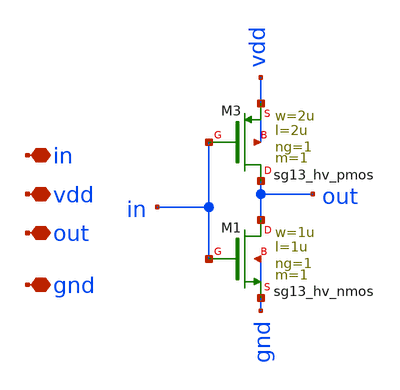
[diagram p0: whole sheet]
** sch_path: Clock_gen_using_transistor_hv/inverter.sch
**.subckt inverter in vdd out gnd
*.iopin in
*.iopin vdd
*.iopin out
*.iopin gnd
XM3 out in vdd vdd sg13_hv_pmos w=2u l=2u ng=1 m=1 mm_ok=1
XM1 out in gnd gnd sg13_hv_nmos w=1u l=1u ng=1 m=1 mm_ok=1
**.ends
.end
